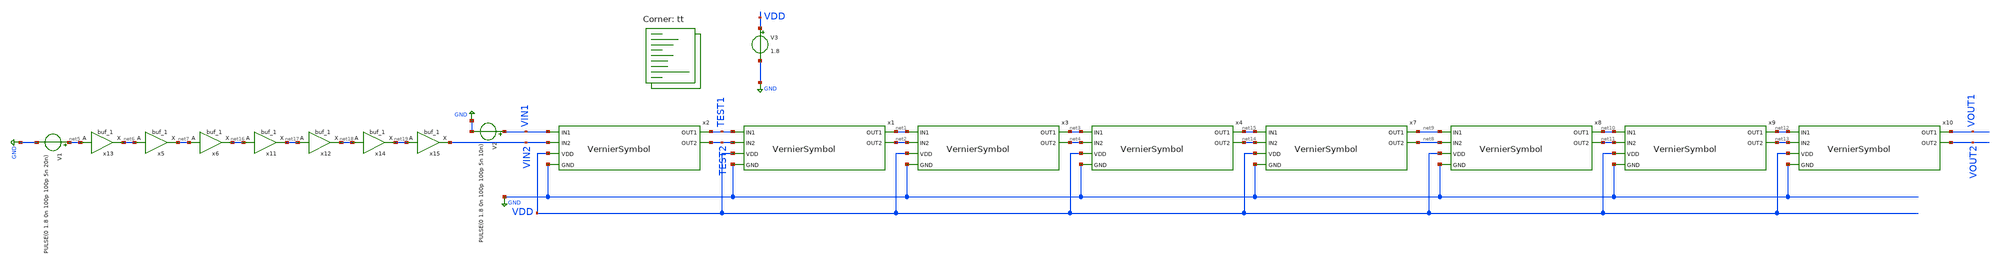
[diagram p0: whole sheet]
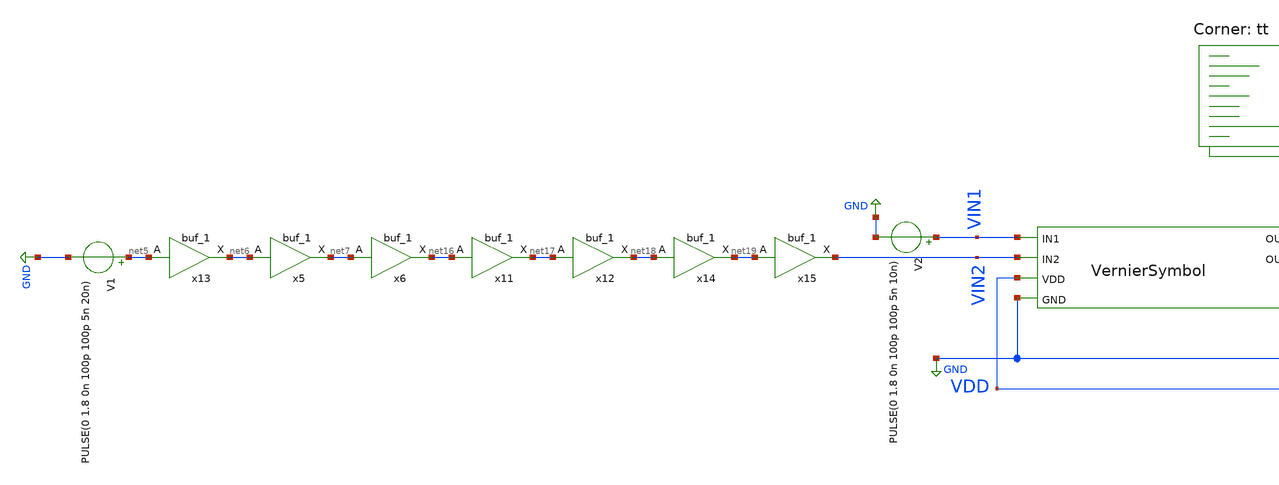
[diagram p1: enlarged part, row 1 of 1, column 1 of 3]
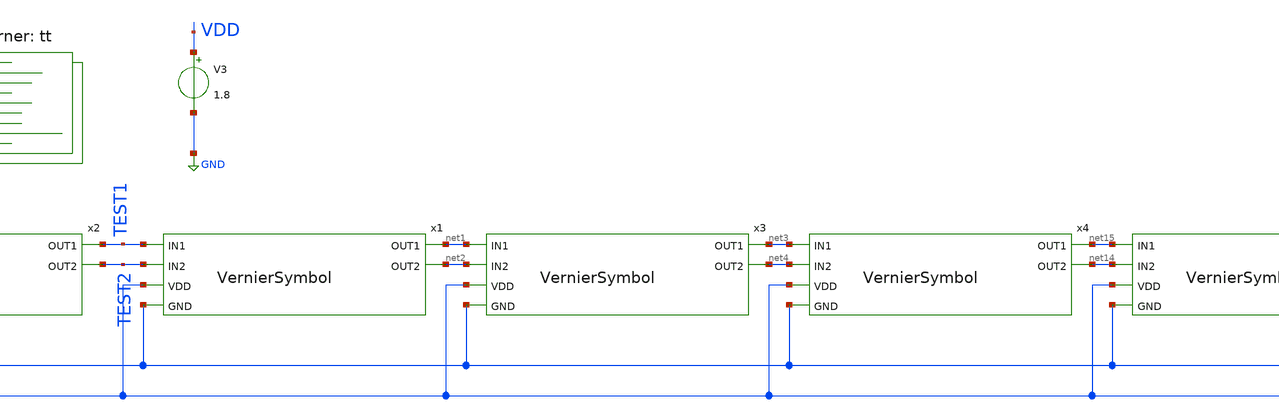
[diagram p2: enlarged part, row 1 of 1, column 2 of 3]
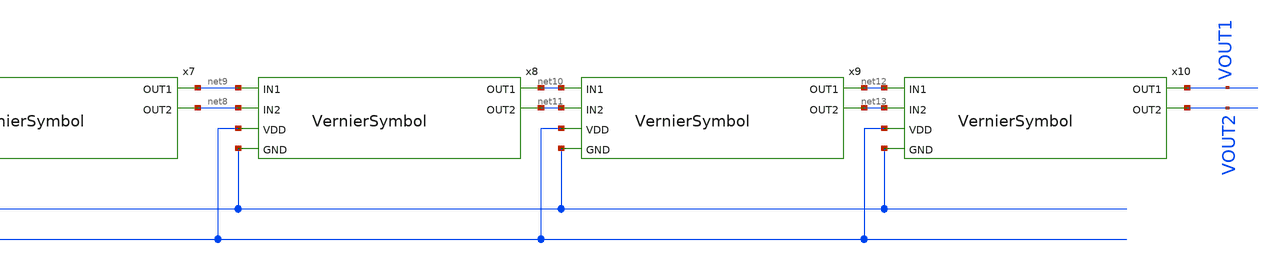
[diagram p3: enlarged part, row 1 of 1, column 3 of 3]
** sch_path: xschem/projects/VernierArray.sch
**.subckt VernierArray
V1 net5 GND PULSE(0 1.8 0n 100p 100p 5n 20n)
V2 VIN1 GND PULSE(0 1.8 0n 100p 100p 5n 10n)
V3 VDD GND 1.8
x13 net5 GND GND VDD VDD net6 sky130_fd_sc_hd__buf_1
x5 net6 GND GND VDD VDD net7 sky130_fd_sc_hd__buf_1
x6 net7 GND GND VDD VDD net16 sky130_fd_sc_hd__buf_1
x1 net1 TEST1 net2 TEST2 VDD GND VernierSymbol
x2 TEST1 VIN1 TEST2 VIN2 VDD GND VernierSymbol
x3 net3 net1 net4 net2 VDD GND VernierSymbol
x4 net15 net3 net14 net4 VDD GND VernierSymbol
x7 net9 net15 net8 net14 VDD GND VernierSymbol
x8 net10 net9 net11 net8 VDD GND VernierSymbol
x9 net12 net10 net13 net11 VDD GND VernierSymbol
x10 VOUT1 net12 VOUT2 net13 VDD GND VernierSymbol
x11 net16 GND GND VDD VDD net17 sky130_fd_sc_hd__buf_1
x12 net17 GND GND VDD VDD net18 sky130_fd_sc_hd__buf_1
x14 net18 GND GND VDD VDD net19 sky130_fd_sc_hd__buf_1
x15 net19 GND GND VDD VDD VIN2 sky130_fd_sc_hd__buf_1
**** begin user architecture code


.include $PDK_ROOT/sky130B/libs.ref/sky130_fd_sc_hd/spice/sky130_fd_sc_hd.spice

.control
tran 10p 100n
write VernierDelay.raw
plot v(VOUT1) v(VOUT2)
.endc

.options acct list
.option numdgt=6


.lib $::SKYWATER_MODELS/sky130.lib.spice tt
**** end user architecture code
**.ends

* expanding   symbol:  VernierSymbol.sym # of pins=6
** sym_path: xschem/projects/VernierSymbol.sym
** sch_path: xschem/projects/VernierSymbol.sch
.subckt VernierSymbol OUT1 IN1 OUT2 IN2 VDD GND
*.ipin VDD
*.ipin GND
*.ipin IN1
*.ipin IN2
*.opin OUT1
*.opin OUT2
x2 net11 OUT2 0 0 VDD VDD OUT1 sky130_fd_sc_hd__dlxtp_1
x10 net5 GND GND VDD VDD net10 sky130_fd_sc_hd__buf_1
x11 net4 GND GND VDD VDD net5 sky130_fd_sc_hd__buf_1
x12 IN2 GND GND VDD VDD net4 sky130_fd_sc_hd__buf_1
x6 net3 GND GND VDD VDD net9 sky130_fd_sc_hd__buf_1
x7 net2 GND GND VDD VDD net3 sky130_fd_sc_hd__buf_1
x8 net1 GND GND VDD VDD net2 sky130_fd_sc_hd__buf_1
x9 IN1 GND GND VDD VDD net1 sky130_fd_sc_hd__buf_1
x1 net8 GND GND VDD VDD net11 sky130_fd_sc_hd__buf_1
x3 net7 GND GND VDD VDD net8 sky130_fd_sc_hd__buf_1
x4 net6 GND GND VDD VDD net7 sky130_fd_sc_hd__buf_1
x5 net9 GND GND VDD VDD net6 sky130_fd_sc_hd__buf_1
x13 net10 GND GND VDD VDD OUT2 sky130_fd_sc_hd__buf_1
.ends

.GLOBAL GND
.end
